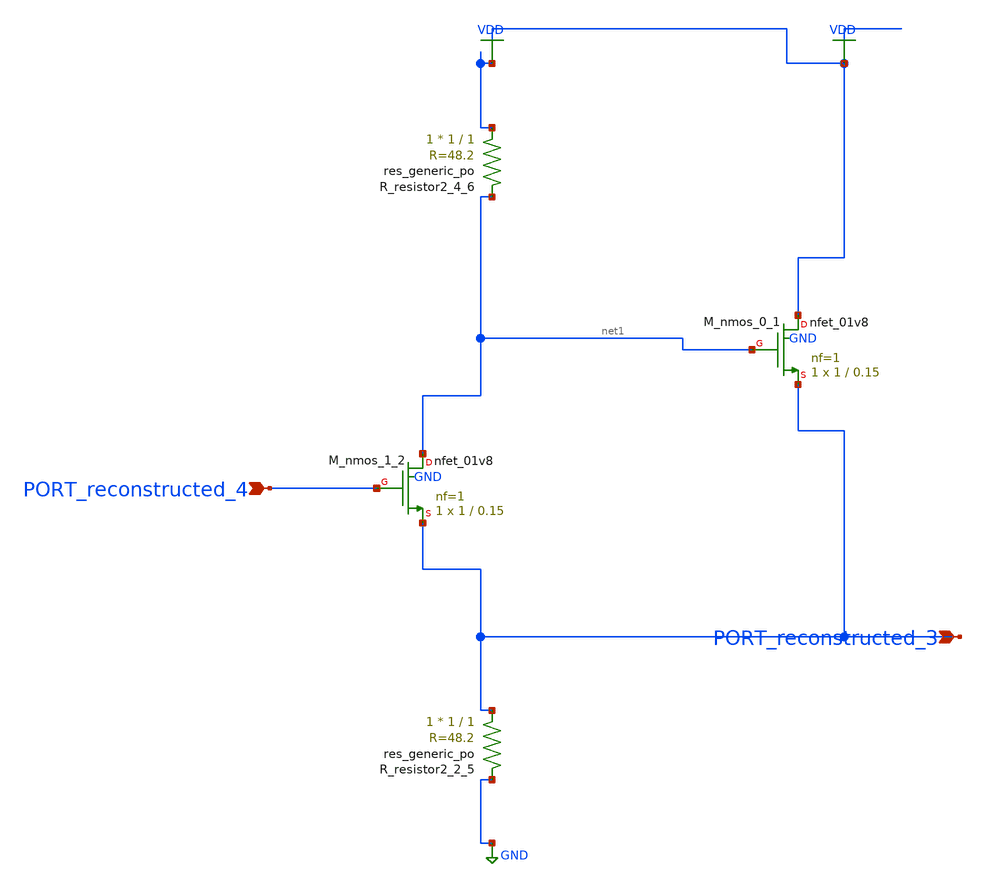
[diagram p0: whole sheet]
** sch_path: schematics/AMSNet/592.sch
**.subckt 592 PORT_reconstructed_4 PORT_reconstructed_3
*.ipin PORT_reconstructed_4
*.ipin PORT_reconstructed_3
XM_nmos_0_1 VDD net1 PORT_reconstructed_3 GND sky130_fd_pr__nfet_01v8 L=0.15 W=1 nf=1 ad='int((1 + 1)/2) * 1 / 1 * 0.29'
+ as='int((1 + 2)/2) * 1 / 1 * 0.29' pd='2*int((1 + 1)/2) * (1 / 1 + 0.29)' ps='2*int((1 + 2)/2) * (1 / 1 + 0.29)'
+ nrd='0.29 / 1 ' nrs='0.29 / 1 ' sa=0 sb=0 sd=0 mult=1 m=1
XM_nmos_1_2 net1 PORT_reconstructed_4 PORT_reconstructed_3 GND sky130_fd_pr__nfet_01v8 L=0.15 W=1 nf=1
+ ad='int((1 + 1)/2) * 1 / 1 * 0.29' as='int((1 + 2)/2) * 1 / 1 * 0.29' pd='2*int((1 + 1)/2) * (1 / 1 + 0.29)'
+ ps='2*int((1 + 2)/2) * (1 / 1 + 0.29)' nrd='0.29 / 1 ' nrs='0.29 / 1 ' sa=0 sb=0 sd=0 mult=1 m=1
XR_resistor2_2_5 PORT_reconstructed_3 GND sky130_fd_pr__res_generic_po W=1 L=1 m=1
XR_resistor2_4_6 VDD net1 sky130_fd_pr__res_generic_po W=1 L=1 m=1
**.ends
.GLOBAL GND
.GLOBAL VDD
.end
